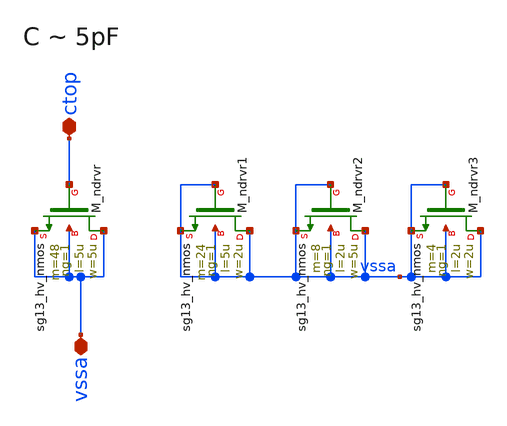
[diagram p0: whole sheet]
** sch_path: Schematics_Layout/sunrise_cfilt/sunrise_cfilt.sch
**.subckt sunrise_cfilt ctop vssa
*.iopin ctop
*.iopin vssa
XM_ndrvr vssa ctop vssa vssa sg13_hv_nmos w=5u l=5u ng=1 m=48 mm_ok=1
XM_ndrvr1 vssa vssa vssa vssa sg13_hv_nmos w=2u l=5u ng=1 m=24 mm_ok=1
XM_ndrvr2 vssa vssa vssa vssa sg13_hv_nmos w=5u l=2u ng=1 m=8 mm_ok=1
XM_ndrvr3 vssa vssa vssa vssa sg13_hv_nmos w=2u l=2u ng=1 m=4 mm_ok=1
**.ends
.end
